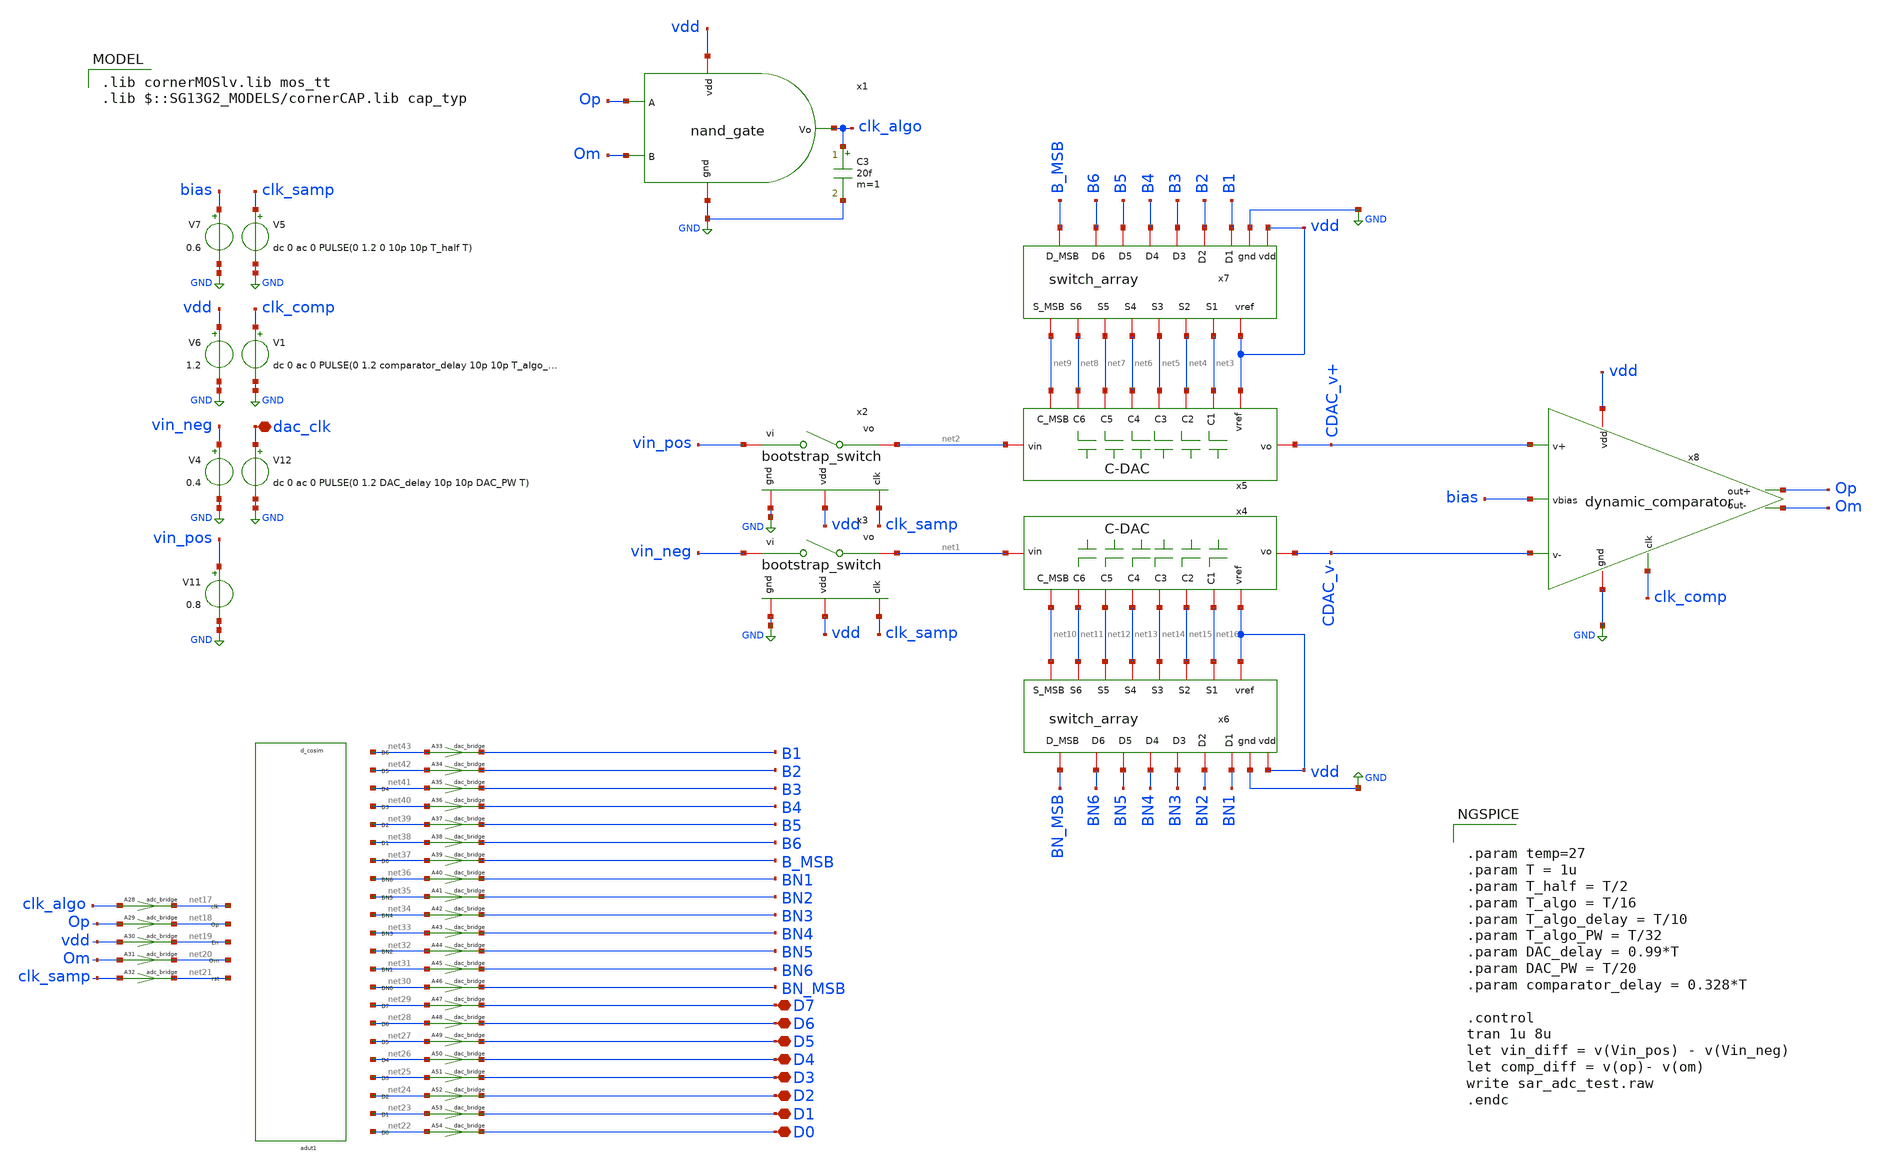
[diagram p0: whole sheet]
** sch_path: dependencies/ADC/ADC-main/schematic/xschem/sar_adc_tutorial.sch
**.subckt sar_adc_tutorial dac_clk D6 D5 D4 D3 D2 D1 D0 D7
*.iopin dac_clk
*.iopin D6
*.iopin D5
*.iopin D4
*.iopin D3
*.iopin D2
*.iopin D1
*.iopin D0
*.iopin D7
V1 clk_comp GND dc 0 ac 0 PULSE(0 1.2 comparator_delay 10p 10p T_algo_PW T_algo)
V6 vdd GND 1.2
V7 bias GND 0.6
V12 dac_clk GND dc 0 ac 0 PULSE(0 1.2 DAC_delay 10p 10p DAC_PW T)
V11 vin_pos GND 0.8
V4 vin_neg GND 0.4
V5 clk_samp GND dc 0 ac 0 PULSE(0 1.2 0 10p 10p T_half T)
C3 clk_algo GND 20f m=1
x8 vdd bias CDAC_v+ CDAC_v- Om Op clk_comp GND dynamic_comparator
adut1 [ net17 net18 net19 net20 net21 ] [ net43 net42 net41 net40 net39 net38 net37 net36 net35
+ net34 net33 net32 net31 net30 net29 net28 net27 net26 net25 net24 net23 net22 ] null dut
.model dut d_cosim simulation=./sar_logic.so
A28 [ clk_algo ] [ net17 ] adc1
.model adc1 adc_bridge in_low=0.4 in_high=0.6
A29 [ Op ] [ net18 ] adc1
.model adc1 adc_bridge in_low=0.4 in_high=0.6
A30 [ vdd ] [ net19 ] adc1
.model adc1 adc_bridge in_low=0.4 in_high=0.6
A31 [ Om ] [ net20 ] adc1
.model adc1 adc_bridge in_low=0.4 in_high=0.6
A32 [ clk_samp ] [ net21 ] adc1
.model adc1 adc_bridge in_low=0.4 in_high=0.6
A33 [ net43 ] [ B1 ] dac1
.model dac1 dac_bridge out_low=0 out_high=1.2
A34 [ net42 ] [ B2 ] dac1
.model dac1 dac_bridge out_low=0 out_high=1.2
A35 [ net41 ] [ B3 ] dac1
.model dac1 dac_bridge out_low=0 out_high=1.2
A36 [ net40 ] [ B4 ] dac1
.model dac1 dac_bridge out_low=0 out_high=1.2
A37 [ net39 ] [ B5 ] dac1
.model dac1 dac_bridge out_low=0 out_high=1.2
A38 [ net38 ] [ B6 ] dac1
.model dac1 dac_bridge out_low=0 out_high=1.2
A39 [ net37 ] [ B_MSB ] dac1
.model dac1 dac_bridge out_low=0 out_high=1.2
A40 [ net36 ] [ BN1 ] dac1
.model dac1 dac_bridge out_low=0 out_high=1.2
A41 [ net35 ] [ BN2 ] dac1
.model dac1 dac_bridge out_low=0 out_high=1.2
A42 [ net34 ] [ BN3 ] dac1
.model dac1 dac_bridge out_low=0 out_high=1.2
A43 [ net33 ] [ BN4 ] dac1
.model dac1 dac_bridge out_low=0 out_high=1.2
A44 [ net32 ] [ BN5 ] dac1
.model dac1 dac_bridge out_low=0 out_high=1.2
A45 [ net31 ] [ BN6 ] dac1
.model dac1 dac_bridge out_low=0 out_high=1.2
A46 [ net30 ] [ BN_MSB ] dac1
.model dac1 dac_bridge out_low=0 out_high=1.2
A47 [ net29 ] [ D7 ] dac1
.model dac1 dac_bridge out_low=0 out_high=1.2
A48 [ net28 ] [ D6 ] dac1
.model dac1 dac_bridge out_low=0 out_high=1.2
A49 [ net27 ] [ D5 ] dac1
.model dac1 dac_bridge out_low=0 out_high=1.2
A50 [ net26 ] [ D4 ] dac1
.model dac1 dac_bridge out_low=0 out_high=1.2
A51 [ net25 ] [ D3 ] dac1
.model dac1 dac_bridge out_low=0 out_high=1.2
A52 [ net24 ] [ D2 ] dac1
.model dac1 dac_bridge out_low=0 out_high=1.2
A53 [ net23 ] [ D1 ] dac1
.model dac1 dac_bridge out_low=0 out_high=1.2
A54 [ net22 ] [ D0 ] dac1
.model dac1 dac_bridge out_low=0 out_high=1.2
x1 vdd clk_algo Om Op GND nand_gate
x2 vdd vin_pos net2 clk_samp GND bootstrap_switch
x3 vdd vin_neg net1 clk_samp GND bootstrap_switch
x4 net1 CDAC_v- net12 net11 net14 net13 net15 net16 vdd net10 C-DAC
x5 net2 CDAC_v+ net7 net8 net5 net6 net4 net3 vdd net9 C-DAC
x6 vdd vdd GND net12 net11 BN5 BN6 net10 BN_MSB net16 net15 BN1 BN2 net14 BN3 net13 BN4 switch_array
x7 vdd vdd GND net7 net8 B5 B6 net9 B_MSB net3 net4 B1 B2 net5 B3 net6 B4 switch_array
**** begin user architecture code


.param temp=27
.param T = 1u
.param T_half = T/2
.param T_algo = T/16
.param T_algo_delay = T/10
.param T_algo_PW = T/32
.param DAC_delay = 0.99*T
.param DAC_PW = T/20
.param comparator_delay = 0.328*T

.control
tran 1u 8u
let vin_diff = v(Vin_pos) - v(Vin_neg)
let comp_diff = v(op)- v(om)
write sar_adc_test.raw
.endc


 .lib cornerMOSlv.lib mos_tt
.lib $::SG13G2_MODELS/cornerCAP.lib cap_typ

**** end user architecture code
**.ends
.GLOBAL GND
.end
